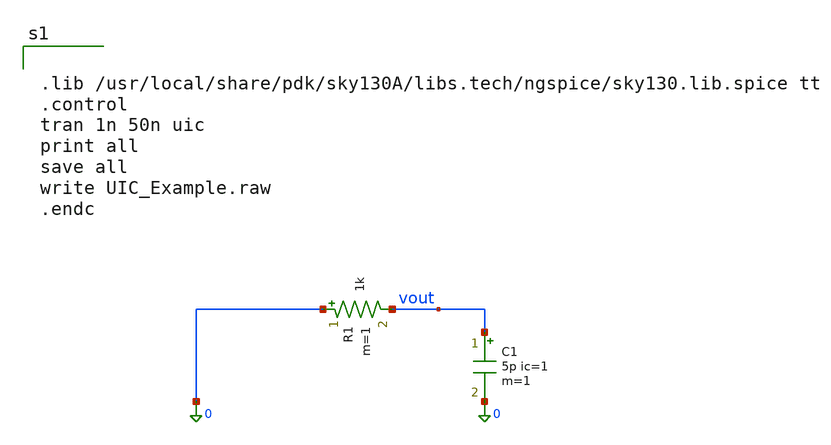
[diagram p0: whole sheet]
** sch_path: mag/layout/UIC_Example.sch
**.subckt UIC_Example
R1 0 vout 1k m=1
C1 vout 0 5p ic=1 m=1
**** begin user architecture code


.lib /usr/local/share/pdk/sky130A/libs.tech/ngspice/sky130.lib.spice tt
.control
tran 1n 50n uic
print all
save all
write UIC_Example.raw
.endc

**** end user architecture code
**.ends
.end
